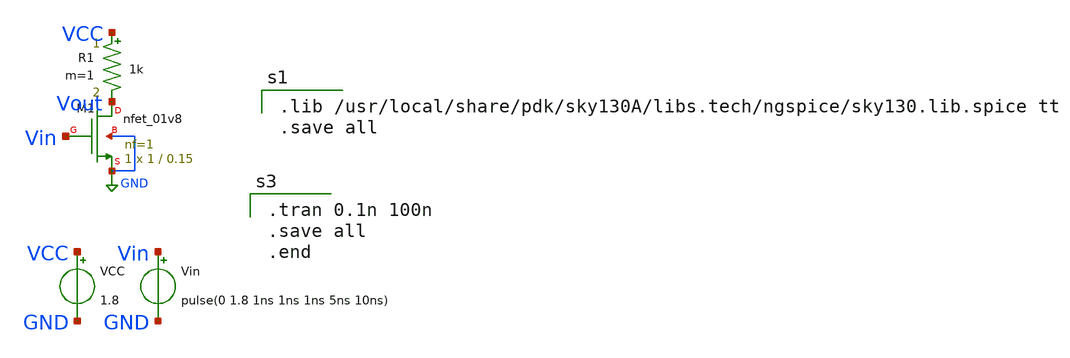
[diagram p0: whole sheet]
** sch_path: Schematic/nmos.sch
**.subckt nmos
VCC VCC GND 1.8
Vin Vin GND pulse(0 1.8 1ns 1ns 1ns 5ns 10ns)
XM1 Vout Vin GND GND sky130_fd_pr__nfet_01v8 L=0.15 W=1 nf=1 ad='int((nf+1)/2) * W/nf * 0.29' as='int((nf+2)/2) * W/nf * 0.29'
+ pd='2*int((nf+1)/2) * (W/nf + 0.29)' ps='2*int((nf+2)/2) * (W/nf + 0.29)' nrd='0.29 / W' nrs='0.29 / W'
+ sa=0 sb=0 sd=0 mult=1 m=1
R1 VCC Vout 1k m=1
**** begin user architecture code

.lib /usr/local/share/pdk/sky130A/libs.tech/ngspice/sky130.lib.spice tt
.save all


.tran 0.1n 100n
.save all
.end

**** end user architecture code
**.ends
.GLOBAL GND
.end
